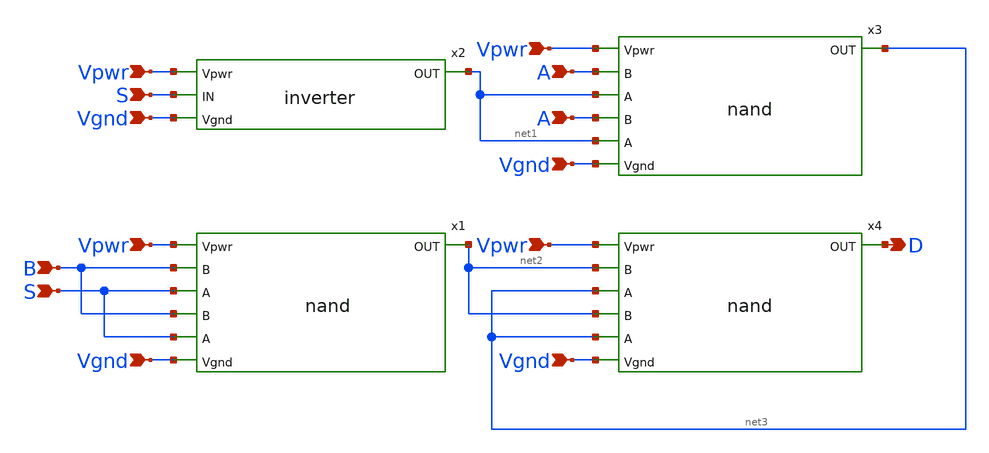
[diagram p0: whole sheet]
** sch_path: MUXDFF/Gates/Mux/mux.sch
**.subckt mux Vpwr B S Vgnd Vpwr Vgnd S Vgnd Vpwr A A Vpwr Vgnd D
*.ipin Vpwr
*.ipin B
*.ipin S
*.ipin Vgnd
*.ipin Vpwr
*.ipin Vgnd
*.ipin S
*.ipin Vgnd
*.ipin Vpwr
*.ipin A
*.ipin A
*.ipin Vpwr
*.ipin Vgnd
*.opin D
x1 Vpwr B S net2 Vgnd nand
x2 Vpwr S net1 Vgnd inverter
x3 Vpwr A net1 net3 Vgnd nand
x4 Vpwr net2 net3 D Vgnd nand
**.ends
.end
